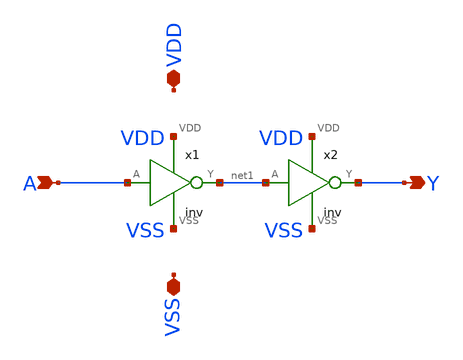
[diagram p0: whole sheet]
** sch_path: examples/ihp-inv/libs/cells/buf/schematic/buf.sch
**.subckt buf A Y VDD VSS
*.ipin A
*.opin Y
*.iopin VDD
*.iopin VSS
x1 A net1 VDD VSS inv
x2 net1 Y VDD VSS inv
**.ends
.end
